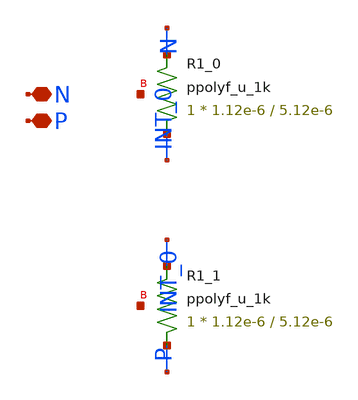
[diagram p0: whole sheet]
** sch_path: design/LELO_TR_GF180MCUD/LELOTR_RES2.sch
**.subckt LELOTR_RES2 N P
*.iopin N
*.iopin P
XR1_0 INT_0 N net1 ppolyf_u_1k r_width=1.12e-6 r_length=5.12e-6 m=1
XR1_1 P INT_0 net2 ppolyf_u_1k r_width=1.12e-6 r_length=5.12e-6 m=1
**.ends
.end
